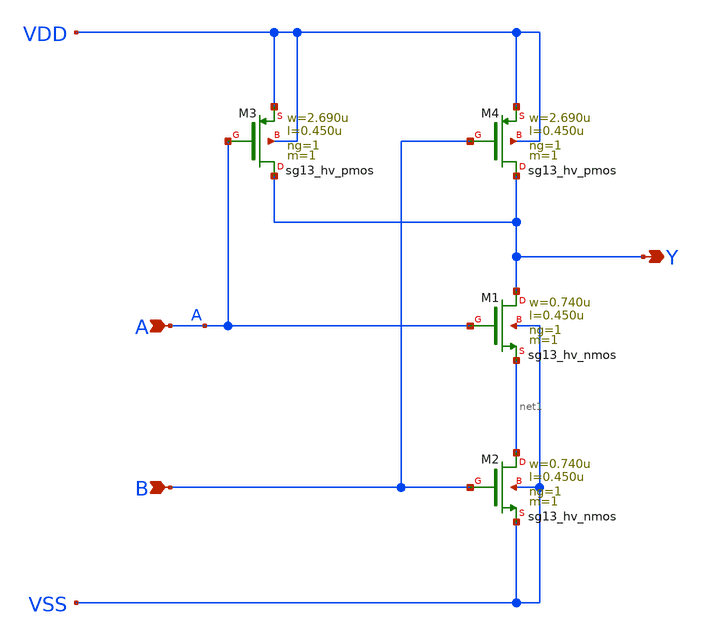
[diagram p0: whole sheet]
** sch_path: ihp-sg13g2/libs.ref/sg13g2_stdcell_hv/sch/xschem/sg13g2_hv_nand2_1.sch
* Copyright 2023 IHP PDK Authors
* Licensed under the Apache License, Version 2.0 (the "License");
* you may not use this file except in compliance with the License.
* You may obtain a copy of the License at
* https://www.apache.org/licenses/LICENSE-2.0
* Unless required by applicable law or agreed to in writing, software
* distributed under the License is distributed on an "AS IS" BASIS,
* WITHOUT WARRANTIES OR CONDITIONS OF ANY KIND, either express or implied.
* See the License for the specific language governing permissions and
* limitations under the License.
**.subckt sg13g2_hv_nand2_1 A B Y
*.ipin A
*.ipin B
*.opin Y
XM1 Y A net1 VSS sg13_hv_nmos w=0.740u l=0.450u ng=1 m=1 mm_ok=1
XM2 net1 B VSS VSS sg13_hv_nmos w=0.740u l=0.450u ng=1 m=1 mm_ok=1
XM3 Y A VDD VDD sg13_hv_pmos w=2.690u l=0.450u ng=1 m=1 mm_ok=1
XM4 Y B VDD VDD sg13_hv_pmos w=2.690u l=0.450u ng=1 m=1 mm_ok=1
**.ends
.end
